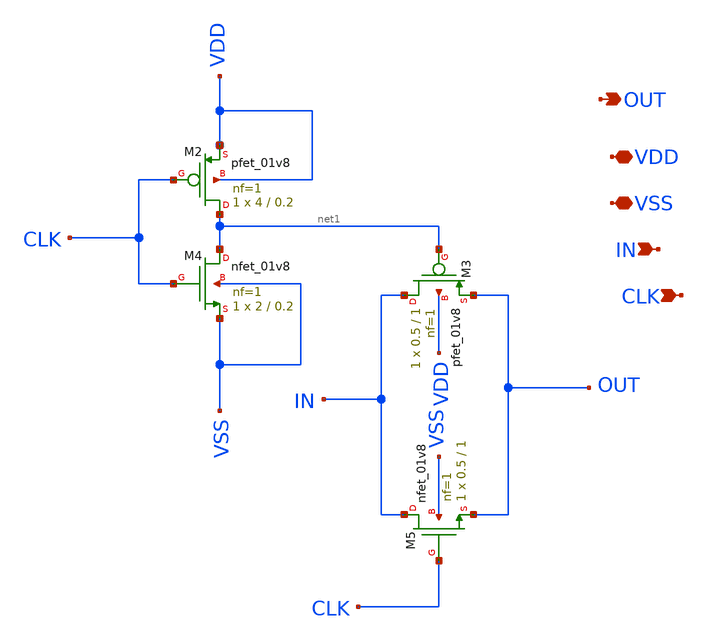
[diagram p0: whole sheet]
** sch_path: Xschem/PLL_TOP_Schematics/TR_Gate_CP.sch
**.subckt TR_Gate_CP VDD VSS IN OUT CLK
*.iopin VDD
*.iopin VSS
*.ipin IN
*.opin OUT
*.ipin CLK
XM2 net1 CLK VDD VDD sky130_fd_pr__pfet_01v8 L=0.2 W=4 nf=1 ad='int((nf+1)/2) * W/nf * 0.29' as='int((nf+2)/2) * W/nf * 0.29'
+ pd='2*int((nf+1)/2) * (W/nf + 0.29)' ps='2*int((nf+2)/2) * (W/nf + 0.29)' nrd='0.29 / W' nrs='0.29 / W'
+ sa=0 sb=0 sd=0 mult=1 m=1
XM3 IN net1 OUT VDD sky130_fd_pr__pfet_01v8 L=1 W=0.5 nf=1 ad='int((nf+1)/2) * W/nf * 0.29' as='int((nf+2)/2) * W/nf * 0.29'
+ pd='2*int((nf+1)/2) * (W/nf + 0.29)' ps='2*int((nf+2)/2) * (W/nf + 0.29)' nrd='0.29 / W' nrs='0.29 / W'
+ sa=0 sb=0 sd=0 mult=1 m=1
XM4 net1 CLK VSS VSS sky130_fd_pr__nfet_01v8 L=0.2 W=2 nf=1 ad='int((nf+1)/2) * W/nf * 0.29' as='int((nf+2)/2) * W/nf * 0.29'
+ pd='2*int((nf+1)/2) * (W/nf + 0.29)' ps='2*int((nf+2)/2) * (W/nf + 0.29)' nrd='0.29 / W' nrs='0.29 / W'
+ sa=0 sb=0 sd=0 mult=1 m=1
XM5 IN CLK OUT VSS sky130_fd_pr__nfet_01v8 L=1 W=0.5 nf=1 ad='int((nf+1)/2) * W/nf * 0.29' as='int((nf+2)/2) * W/nf * 0.29'
+ pd='2*int((nf+1)/2) * (W/nf + 0.29)' ps='2*int((nf+2)/2) * (W/nf + 0.29)' nrd='0.29 / W' nrs='0.29 / W'
+ sa=0 sb=0 sd=0 mult=1 m=1
**.ends
.end
